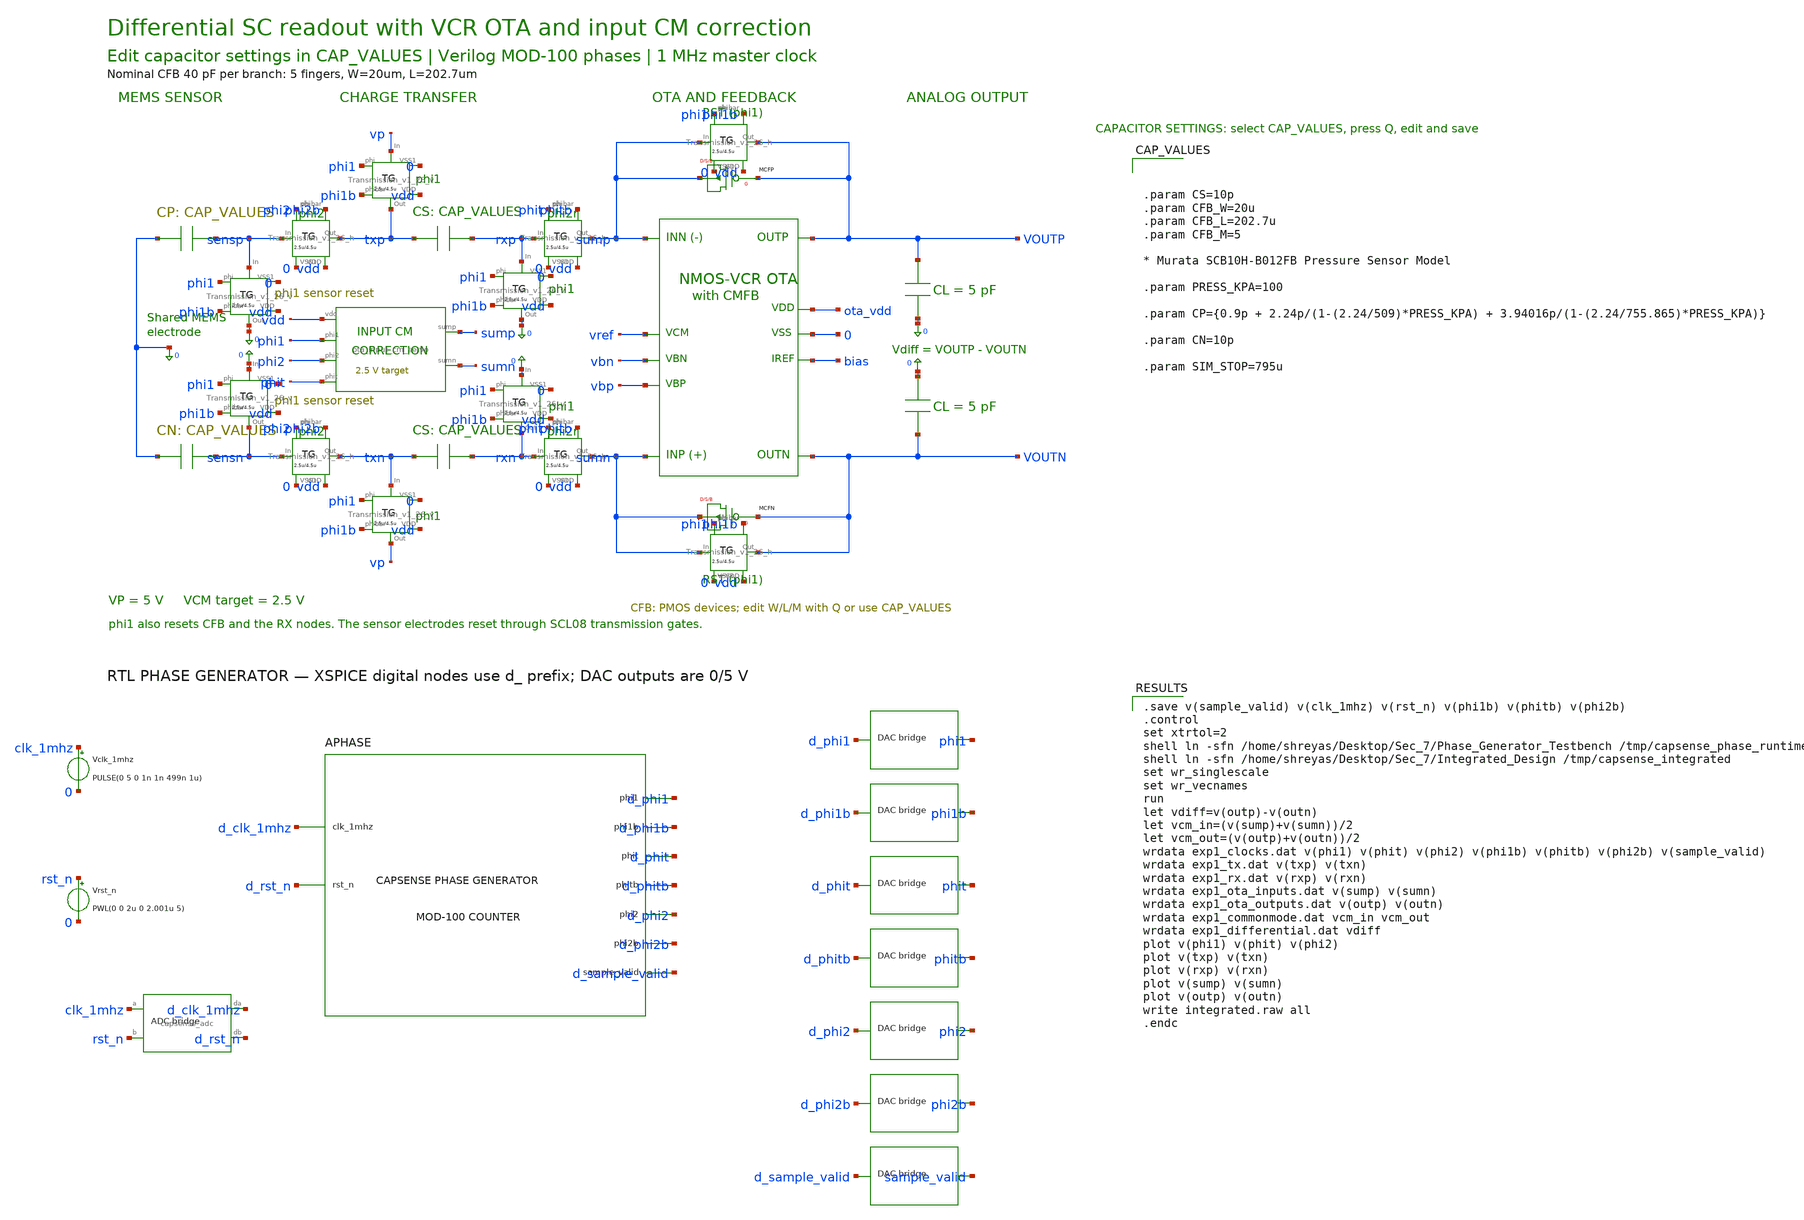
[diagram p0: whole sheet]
** sch_path: Mixed_Signal/Integrated_Design/schematic/capsense_cfb_40pf.sch
**.subckt capsense_cfb_40pf
XOTA sumn sump outp outn ota_vdd 0 bias vref vbn vbp ota_telescopic_cm2p5
CMEMP 0 sensp {CP}
XSENSEP phi2 0 sensp txp vdd phi2b Transmission_v1_26_h
XSRESETP phi1 0 sensp 0 vdd phi1b Transmission_v1_26_v
XCHARGEP phi1 0 vp txp vdd phi1b Transmission_v1_26_v
CSP txp rxp {CS}
XRRESETP phi1 0 rxp 0 vdd phi1b Transmission_v1_26_v
XXFERP phit 0 rxp sump vdd phitb Transmission_v1_26_h
MCFP sump outp sump sump P W={CFB_W} L={CFB_L} M={CFB_M} AD='( {CFB_W} ) * 4.5u' AS='( {CFB_W} ) * 4.5u'
+ PD='2 * ( {CFB_W} ) + 9u' PS='2 * ( {CFB_W} ) + 9u'
XFBRESETP phi1 0 sump outp vdd phi1b Transmission_v1_26_h
CLP outp 0 5p
CMEMN 0 sensn {CN}
XSENSEN phi2 0 sensn txn vdd phi2b Transmission_v1_26_h
XSRESETN phi1 0 0 sensn vdd phi1b Transmission_v1_26_v
XCHARGEN phi1 0 txn vp vdd phi1b Transmission_v1_26_v
CSN txn rxn {CS}
XRRESETN phi1 0 0 rxn vdd phi1b Transmission_v1_26_v
XXFERN phit 0 rxn sumn vdd phitb Transmission_v1_26_h
MCFN sumn outn sumn sumn P W={CFB_W} L={CFB_L} M={CFB_M} AD='( {CFB_W} ) * 4.5u' AS='( {CFB_W} ) * 4.5u'
+ PD='2 * ( {CFB_W} ) + 9u' PS='2 * ( {CFB_W} ) + 9u'
XFBRESETN phi1 0 sumn outn vdd phi1b Transmission_v1_26_h
CLN 0 outn 5p
XICM sump sumn vdd phi1 phi2 phit ota_input_cm_servo
APHASE [ d_clk_1mhz d_rst_n ] [ d_phi1 d_phit d_phi2 d_phi1b d_phitb d_phi2b d_sample_valid ] null
+ capsense_phase_gen_cosim
Vclk_1mhz clk_1mhz 0 PULSE(0 5 0 1n 1n 499n 1u)
Vrst_n rst_n 0 PWL(0 0 2u 0 2.001u 5)
AINPUTS [ clk_1mhz rst_n ] [ d_clk_1mhz d_rst_n ] capsense_adc
ADAC_phi1 [ d_phi1 ] [ phi1 ] capsense_dac
ADAC_phi1b [ d_phi1b ] [ phi1b ] capsense_dac
ADAC_phit [ d_phit ] [ phit ] capsense_dac
ADAC_phitb [ d_phitb ] [ phitb ] capsense_dac
ADAC_phi2 [ d_phi2 ] [ phi2 ] capsense_dac
ADAC_phi2b [ d_phi2b ] [ phi2b ] capsense_dac
ADAC_sample_valid [ d_sample_valid ] [ sample_valid ] capsense_dac
**** begin user architecture code
.include /home/shreyas/Desktop/Sec_7/Integrated_Design/simulation/analog_support.spice
.include /home/shreyas/Desktop/Sec_7/Integrated_Design/simulation/cosim_models.spice

.save v(sample_valid) v(clk_1mhz) v(rst_n) v(phi1b) v(phitb) v(phi2b)
.control
set xtrtol=2
shell ln -sfn /home/shreyas/Desktop/Sec_7/Phase_Generator_Testbench /tmp/capsense_phase_runtime
shell ln -sfn /home/shreyas/Desktop/Sec_7/Integrated_Design /tmp/capsense_integrated
set wr_singlescale
set wr_vecnames
run
let vdiff=v(outp)-v(outn)
let vcm_in=(v(sump)+v(sumn))/2
let vcm_out=(v(outp)+v(outn))/2
wrdata exp1_clocks.dat v(phi1) v(phit) v(phi2) v(phi1b) v(phitb) v(phi2b) v(sample_valid)
wrdata exp1_tx.dat v(txp) v(txn)
wrdata exp1_rx.dat v(rxp) v(rxn)
wrdata exp1_ota_inputs.dat v(sump) v(sumn)
wrdata exp1_ota_outputs.dat v(outp) v(outn)
wrdata exp1_commonmode.dat vcm_in vcm_out
wrdata exp1_differential.dat vdiff
plot v(phi1) v(phit) v(phi2)
plot v(txp) v(txn)
plot v(rxp) v(rxn)
plot v(sump) v(sumn)
plot v(outp) v(outn)
write integrated.raw all
.endc




.param CS=10p
.param CFB_W=20u
.param CFB_L=202.7u
.param CFB_M=5

* Murata SCB10H-B012FB Pressure Sensor Model

.param PRESS_KPA=100

.param CP={0.9p + 2.24p/(1-(2.24/509)*PRESS_KPA) + 3.94016p/(1-(2.24/755.865)*PRESS_KPA)}

.param CN=10p

.param SIM_STOP=795u

**** end user architecture code
**.ends
.end
